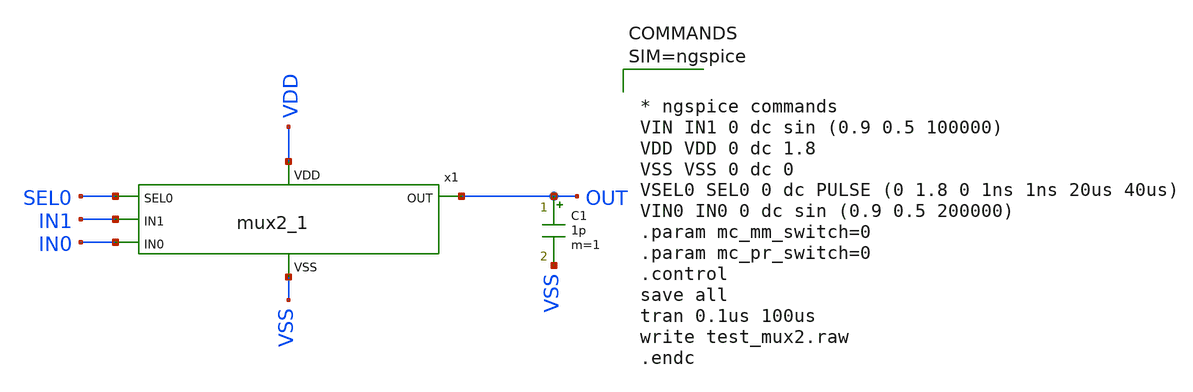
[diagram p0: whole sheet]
** sch_path: xschem/test_mux2.sch
**.subckt test_mux2
x1 SEL0 IN1 OUT IN0 VDD VSS mux2_1
C1 OUT VSS 1p m=1
**** begin user architecture code

** opencircuitdesign pdks install
.lib $::SKYWATER_MODELS/sky130.lib.spice tt





* ngspice commands
VIN IN1 0 dc sin (0.9 0.5 100000)
VDD VDD 0 dc 1.8
VSS VSS 0 dc 0
VSEL0 SEL0 0 dc PULSE (0 1.8 0 1ns 1ns 20us 40us)
VIN0 IN0 0 dc sin (0.9 0.5 200000)
.param mc_mm_switch=0
.param mc_pr_switch=0
.control
save all
tran 0.1us 100us
write test_mux2.raw
.endc


**** end user architecture code
**.ends
.end
